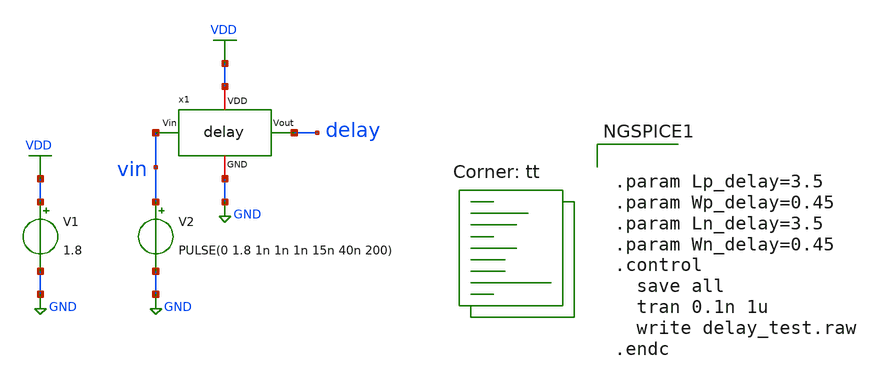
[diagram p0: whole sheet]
** sch_path: SNN/STDP_Circuit_tb.sch
**.subckt STDP_Circuit_tb
V1 VDD GND 1.8
x1 VDD vin delay GND delay
V2 vin GND PULSE(0 1.8 1n 1n 1n 15n 40n 200)
**** begin user architecture code
.lib $::SKYWATER_MODELS/sky130.lib.spice tt

** opencircuitdesign pdks install
.inc $::SKYWATER_MODELS/rram_v0.spice



.param Lp_delay=3.5
.param Wp_delay=0.45
.param Ln_delay=3.5
.param Wn_delay=0.45
.control
  save all
  tran 0.1n 1u
  write delay_test.raw
.endc


**** end user architecture code
**.ends

* expanding   symbol:  /home/ricardo/RATT_repos/Proyectos_xschem/delay/delay.sym # of pins=4
** sym_path: delay/delay.sym
** sch_path: delay/delay.sch
.subckt delay VDD Vin Vout GND
*.ipin Vin
*.opin Vout
*.iopin VDD
*.iopin GND
XM1 net1 Vin VDD VDD sky130_fd_pr__nfet_01v8 L=0.15 W=1 nf=1 ad='int((nf+1)/2) * W/nf * 0.29' as='int((nf+2)/2) * W/nf * 0.29'
+ pd='2*int((nf+1)/2) * (W/nf + 0.29)' ps='2*int((nf+2)/2) * (W/nf + 0.29)' nrd='0.29 / W' nrs='0.29 / W'
+ sa=0 sb=0 sd=0 mult=1 m=1
XM2 net1 Vin GND GND sky130_fd_pr__nfet_01v8 L=0.15 W=1 nf=1 ad='int((nf+1)/2) * W/nf * 0.29' as='int((nf+2)/2) * W/nf * 0.29'
+ pd='2*int((nf+1)/2) * (W/nf + 0.29)' ps='2*int((nf+2)/2) * (W/nf + 0.29)' nrd='0.29 / W' nrs='0.29 / W'
+ sa=0 sb=0 sd=0 mult=1 m=1
XM3 net2 net1 VDD VDD sky130_fd_pr__nfet_01v8 L=0.15 W=1 nf=1 ad='int((nf+1)/2) * W/nf * 0.29' as='int((nf+2)/2) * W/nf * 0.29'
+ pd='2*int((nf+1)/2) * (W/nf + 0.29)' ps='2*int((nf+2)/2) * (W/nf + 0.29)' nrd='0.29 / W' nrs='0.29 / W'
+ sa=0 sb=0 sd=0 mult=1 m=1
XM4 net2 net1 GND GND sky130_fd_pr__nfet_01v8 L=0.15 W=1 nf=1 ad='int((nf+1)/2) * W/nf * 0.29' as='int((nf+2)/2) * W/nf * 0.29'
+ pd='2*int((nf+1)/2) * (W/nf + 0.29)' ps='2*int((nf+2)/2) * (W/nf + 0.29)' nrd='0.29 / W' nrs='0.29 / W'
+ sa=0 sb=0 sd=0 mult=1 m=1
XM5 net3 net2 VDD VDD sky130_fd_pr__nfet_01v8 L=0.15 W=1 nf=1 ad='int((nf+1)/2) * W/nf * 0.29' as='int((nf+2)/2) * W/nf * 0.29'
+ pd='2*int((nf+1)/2) * (W/nf + 0.29)' ps='2*int((nf+2)/2) * (W/nf + 0.29)' nrd='0.29 / W' nrs='0.29 / W'
+ sa=0 sb=0 sd=0 mult=1 m=1
XM6 net3 net2 GND GND sky130_fd_pr__nfet_01v8 L=0.15 W=1 nf=1 ad='int((nf+1)/2) * W/nf * 0.29' as='int((nf+2)/2) * W/nf * 0.29'
+ pd='2*int((nf+1)/2) * (W/nf + 0.29)' ps='2*int((nf+2)/2) * (W/nf + 0.29)' nrd='0.29 / W' nrs='0.29 / W'
+ sa=0 sb=0 sd=0 mult=1 m=1
XM7 Vout net3 VDD VDD sky130_fd_pr__nfet_01v8 L=0.15 W=1 nf=1 ad='int((nf+1)/2) * W/nf * 0.29' as='int((nf+2)/2) * W/nf * 0.29'
+ pd='2*int((nf+1)/2) * (W/nf + 0.29)' ps='2*int((nf+2)/2) * (W/nf + 0.29)' nrd='0.29 / W' nrs='0.29 / W'
+ sa=0 sb=0 sd=0 mult=1 m=1
XM8 Vout net3 GND GND sky130_fd_pr__nfet_01v8 L=0.15 W=1 nf=1 ad='int((nf+1)/2) * W/nf * 0.29' as='int((nf+2)/2) * W/nf * 0.29'
+ pd='2*int((nf+1)/2) * (W/nf + 0.29)' ps='2*int((nf+2)/2) * (W/nf + 0.29)' nrd='0.29 / W' nrs='0.29 / W'
+ sa=0 sb=0 sd=0 mult=1 m=1
.ends

.GLOBAL GND
.GLOBAL VDD
.end
